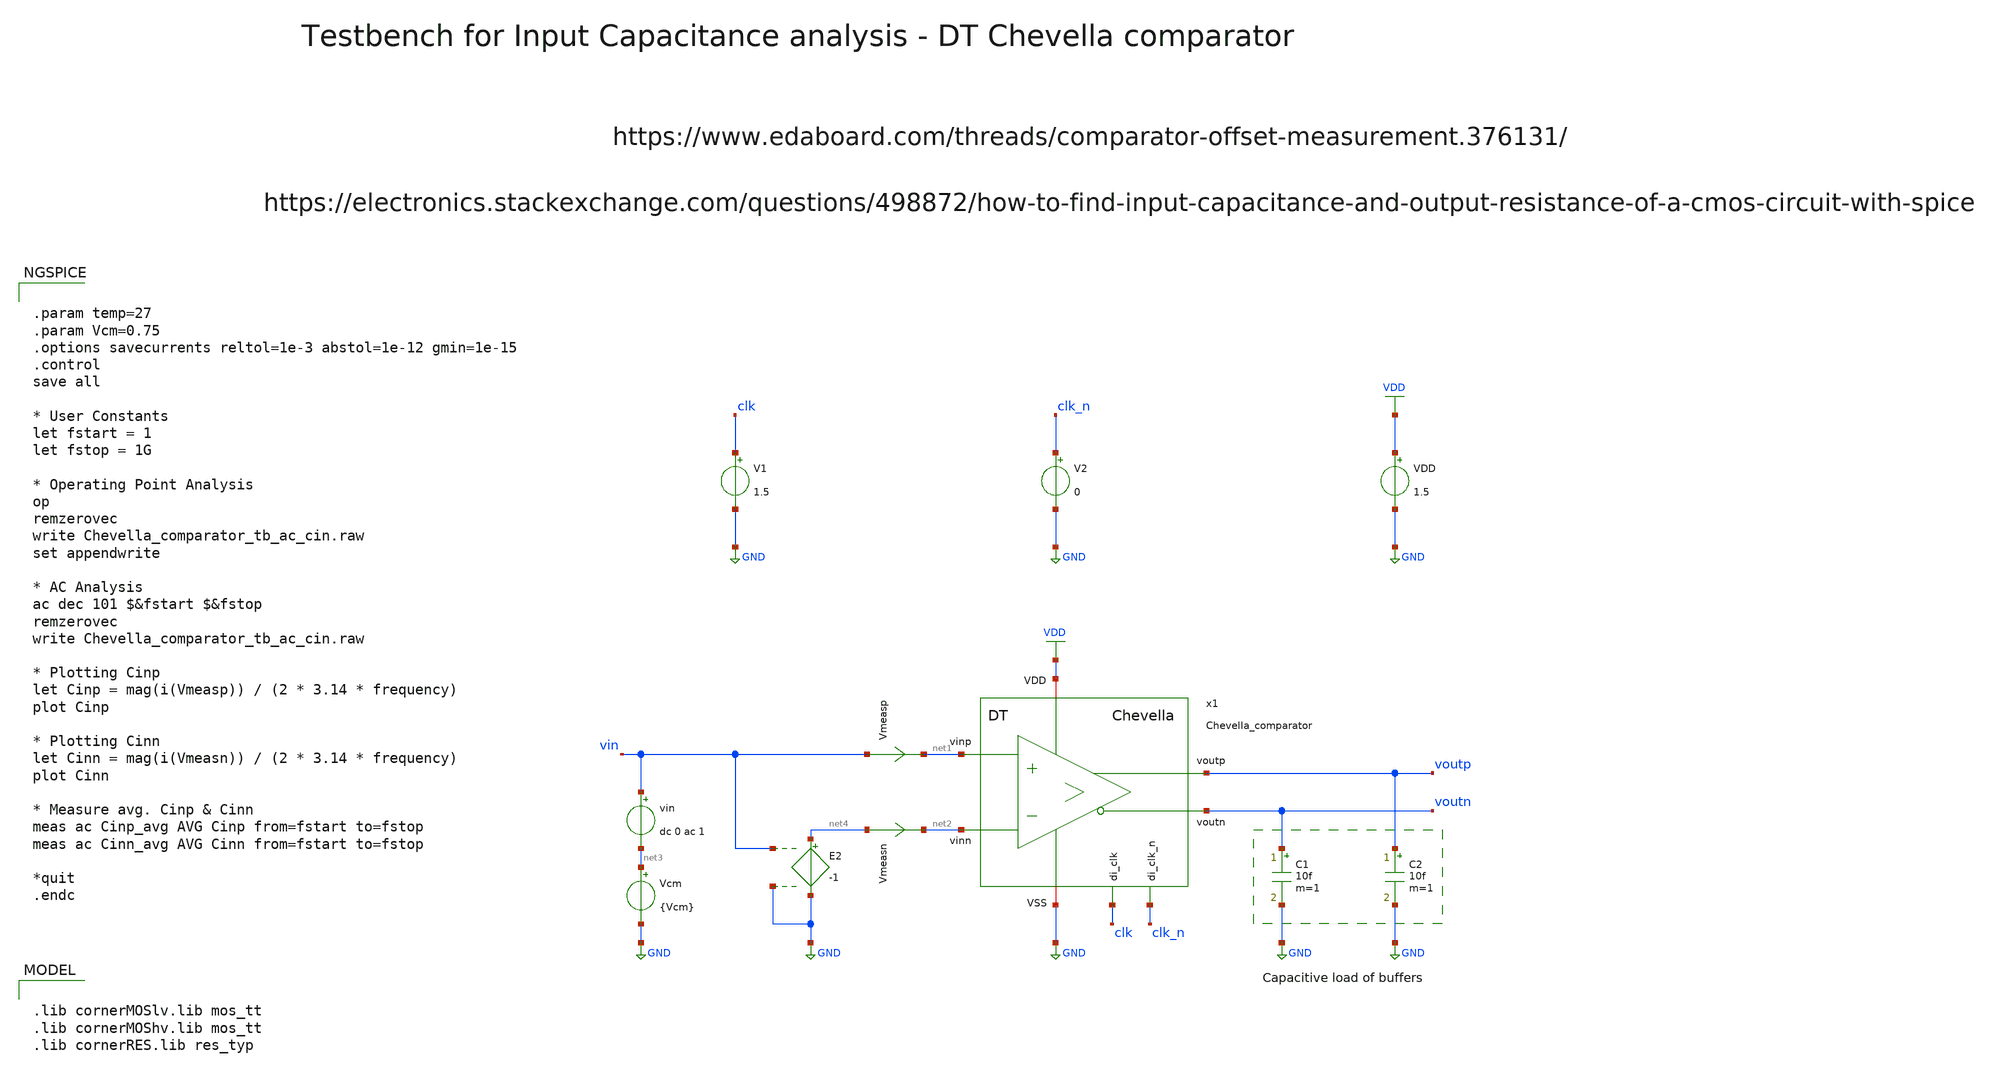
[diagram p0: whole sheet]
** sch_path: SG13G2_ATBS-ADC-main/xschem/comparator/discrete_time/Chevella/testbenches/Chevella_comparator_tb_ac_cin.sch
**.subckt Chevella_comparator_tb_ac_cin
VDD VDD GND 1.5
V1 clk GND 1.5
V2 clk_n GND 0
C1 voutn GND 10f m=1
C2 voutp GND 10f m=1
Vmeasp vin net1 0
.save i(vmeasp)
Vmeasn net4 net2 0
.save i(vmeasn)
vin vin net3 dc 0 ac 1
Vcm net3 GND {Vcm}
E2 net4 GND vin GND -1
x1 clk_n clk VDD voutp net1 GND voutn net2 Chevella_comparator
**** begin user architecture code

.lib cornerMOSlv.lib mos_tt
.lib cornerMOShv.lib mos_tt
.lib cornerRES.lib res_typ



.param temp=27
.param Vcm=0.75
.options savecurrents reltol=1e-3 abstol=1e-12 gmin=1e-15
.control
save all

* User Constants
let fstart = 1
let fstop = 1G

* Operating Point Analysis
op
remzerovec
write Chevella_comparator_tb_ac_cin.raw
set appendwrite

* AC Analysis
ac dec 101 $&fstart $&fstop
remzerovec
write Chevella_comparator_tb_ac_cin.raw

* Plotting Cinp
let Cinp = mag(i(Vmeasp)) / (2 * 3.14 * frequency)
plot Cinp

* Plotting Cinn
let Cinn = mag(i(Vmeasn)) / (2 * 3.14 * frequency)
plot Cinn

* Measure avg. Cinp & Cinn
meas ac Cinp_avg AVG Cinp from=fstart to=fstop
meas ac Cinn_avg AVG Cinn from=fstart to=fstop

*quit
.endc

**** end user architecture code
**.ends

* expanding   symbol:  comparator/discrete_time/Chevella/Chevella_comparator.sym # of pins=8
** sym_path: SG13G2_ATBS-ADC-main/xschem/comparator/discrete_time/Chevella/Chevella_comparator.sym
** sch_path: SG13G2_ATBS-ADC-main/xschem/comparator/discrete_time/Chevella/Chevella_comparator.sch
.subckt Chevella_comparator di_clk_n di_clk VDD voutp vinp VSS voutn vinn
*.iopin VDD
*.opin voutp
*.opin voutn
*.ipin di_clk_n
*.iopin VSS
*.ipin vinp
*.ipin vinn
*.ipin di_clk
XM1a vcpn vinp net1 VSS sg13_lv_nmos w=1.0u l=0.13u ng=1 m=1 mm_ok=1
XM2a vcpp vinn net2 VSS sg13_lv_nmos w=1.0u l=0.13u ng=1 m=1 mm_ok=1
XM3 vs di_clk VSS VSS sg13_lv_nmos w=1.0u l=0.13u ng=1 m=1 mm_ok=1
XM4a vcpn di_clk VDD VDD sg13_lv_pmos w=1.0u l=0.13u ng=1 m=1 mm_ok=1
XM5a vcpp di_clk VDD VDD sg13_lv_pmos w=1.0u l=0.13u ng=1 m=1 mm_ok=1
XM12 voutp di_clk_n VSS VSS sg13_lv_nmos w=1.0u l=0.13u ng=1 m=1 mm_ok=1
XM8 net3 voutn VDD VDD sg13_lv_pmos w=2.0u l=0.13u ng=2 m=1 mm_ok=1
XM10 voutp voutn VSS VSS sg13_lv_nmos w=1.0u l=0.13u ng=1 m=1 mm_ok=1
XM11 voutn voutp VSS VSS sg13_lv_nmos w=1.0u l=0.13u ng=1 m=1 mm_ok=1
XM13 voutn di_clk_n VSS VSS sg13_lv_nmos w=1.0u l=0.13u ng=1 m=1 mm_ok=1
CP1 vcpn VSS 300f m=1
CP2 vcpp VSS 300f m=1
XM9 net4 voutp VDD VDD sg13_lv_pmos w=2.0u l=0.13u ng=2 m=1 mm_ok=1
XM6 voutp vcpn net3 VDD sg13_lv_pmos w=2.0u l=0.13u ng=2 m=1 mm_ok=1
XM7 voutn vcpp net4 VDD sg13_lv_pmos w=2.0u l=0.13u ng=2 m=1 mm_ok=1
XM4b net1 di_clk VDD VDD sg13_lv_pmos w=1.0u l=0.13u ng=1 m=1 mm_ok=1
XM5b net2 di_clk VDD VDD sg13_lv_pmos w=1.0u l=0.13u ng=1 m=1 mm_ok=1
XM1b net1 vcpp vs VSS sg13_lv_nmos w=1.0u l=0.13u ng=1 m=1 mm_ok=1
XM2b net2 vcpn vs VSS sg13_lv_nmos w=1.0u l=0.13u ng=1 m=1 mm_ok=1
.ends

.GLOBAL GND
.GLOBAL VDD
.end
